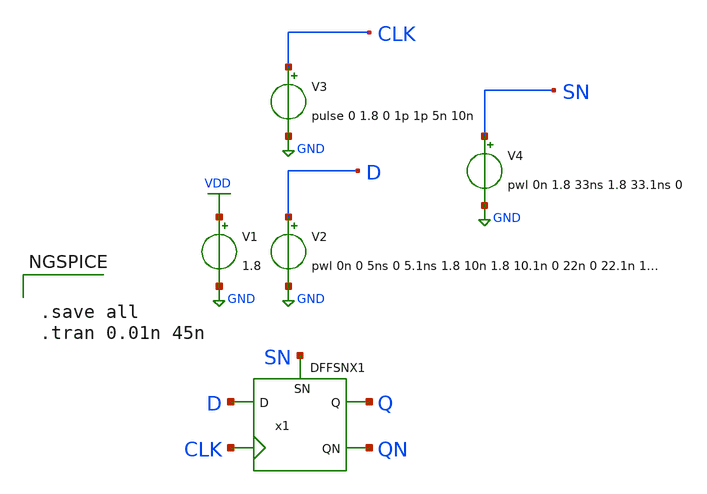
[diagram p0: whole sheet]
** sch_path: lib/xschem/test_DFFSNX1.sch
**.subckt test_DFFSNX1
V2 D GND pwl 0n 0 5ns 0 5.1ns 1.8 10n 1.8 10.1n 0 22n 0 22.1n 1.8 27n 1.8 27.1n 0 34n 0 34.1n 1.8
V1 VDD GND 1.8
V3 CLK GND pulse 0 1.8 0 1p 1p 5n 10n
V4 SN GND pwl 0n 1.8 33ns 1.8 33.1ns 0
x1 Q QN D CLK SN VDD GND DFFSNX1
**** begin user architecture code

.lib $::SKYWATER_MODELS/sky130.lib.spice tt


**** end user architecture code
**.ends
.GLOBAL VDD
.GLOBAL GND
**** begin user architecture code


.save all
.tran 0.01n 45n


**** end user architecture code
.end
